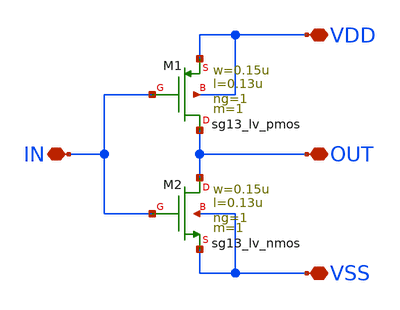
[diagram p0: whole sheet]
** sch_path: blocks/inverter/inverter.sch
**.subckt inverter OUT VDD VSS IN
*.iopin OUT
*.iopin VDD
*.iopin VSS
*.iopin IN
XM1 OUT IN VDD VDD sg13_lv_pmos w=0.15u l=0.13u ng=1 m=1 mm_ok=1
XM2 OUT IN VSS VSS sg13_lv_nmos w=0.15u l=0.13u ng=1 m=1 mm_ok=1
**.ends
.end
